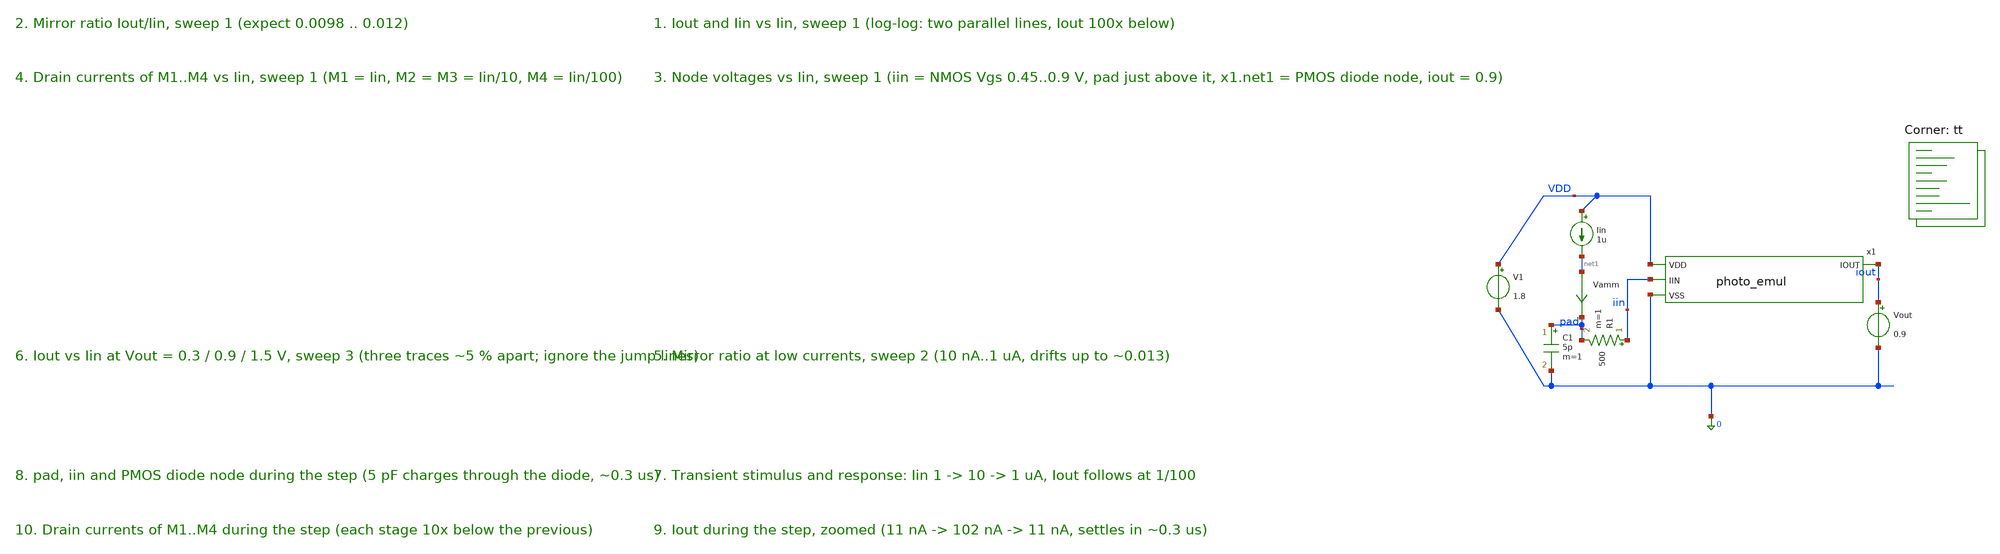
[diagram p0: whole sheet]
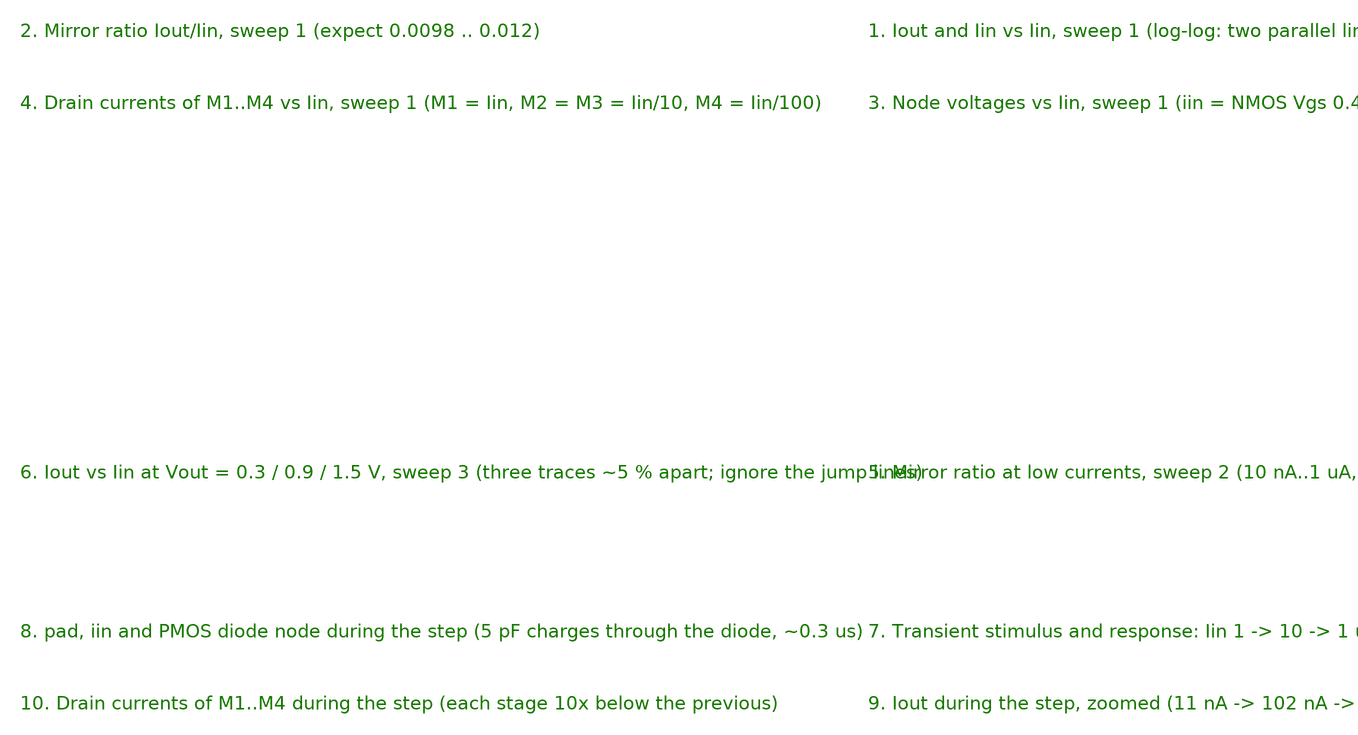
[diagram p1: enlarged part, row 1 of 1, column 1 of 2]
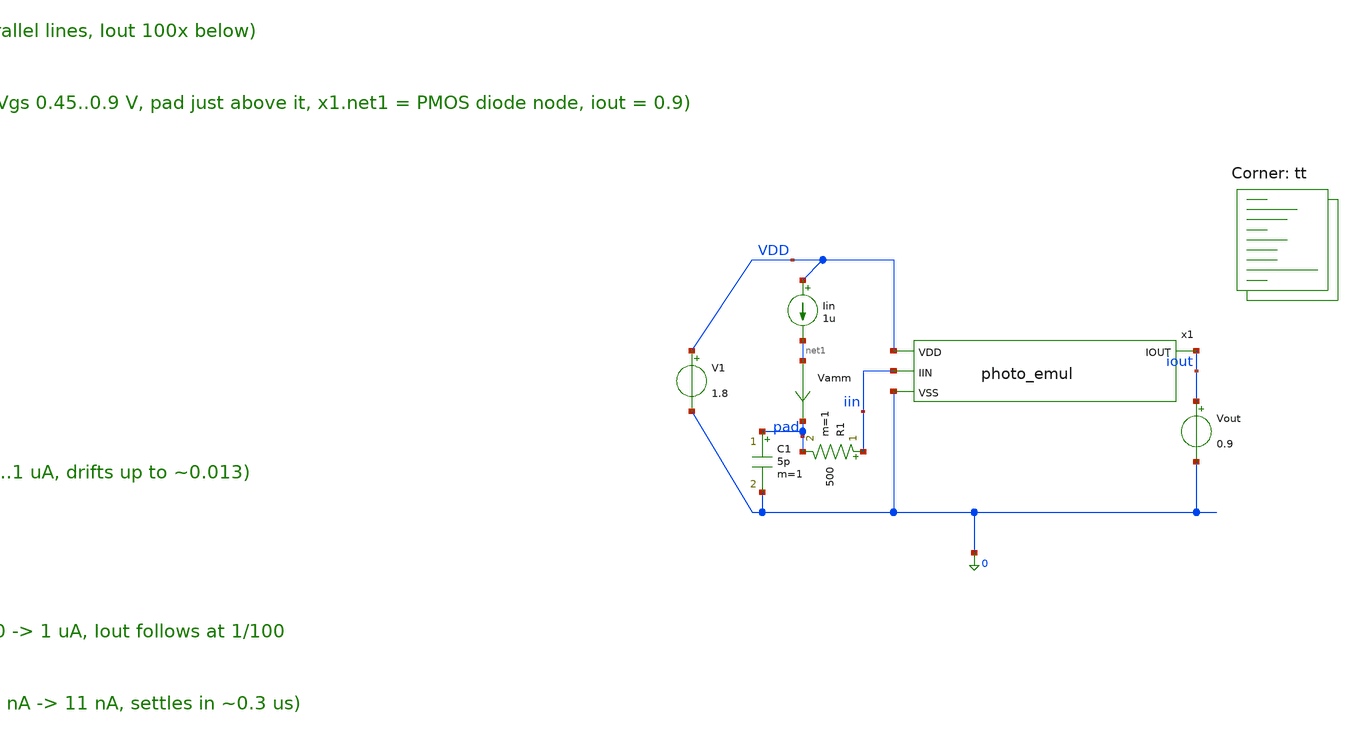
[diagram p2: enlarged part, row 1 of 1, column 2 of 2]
** sch_path: xschem/testbench_emul.sch
**.subckt testbench_emul
x1 VDD iin iout 0 photo_emul
Vamm net1 pad 0
.save i(vamm)
V1 VDD 0 1.8
Iin VDD net1 1u
Vout iout 0 0.9
R1 iin pad 500 m=1
C1 pad 0 5p m=1
**** begin user architecture code
.lib $::SKYWATER_MODELS/sky130.lib.spice tt


.option savecurrents
.control
save all
* sweep 1: input current 100 nA .. 100 uA (linear steps, log axes in the plots)
dc Iin 100n 100u 100n
plot abs(i(vout)) xlog ylog title 'Iout vs Iin (expect Iin/100)'
plot abs(i(vout))/abs(i(vamm)) xlog title 'mirror ratio Iout/Iin (expect 0.01)'
write testbench_emul.raw
set appendwrite
* sweep 2: low end, 10 nA .. 1 uA
dc Iin 10n 1u 10n
plot abs(i(vout))/abs(i(vamm)) xlog title 'mirror ratio at low currents'
write testbench_emul.raw
* sweep 3: same as 1 at Vout = 0.3, 0.9, 1.5 V
dc Iin 100n 100u 100n Vout 0.3 1.5 0.6
plot abs(i(vout)) xlog ylog title 'Iout at Vout = 0.3 / 0.9 / 1.5 V'
write testbench_emul.raw
* transient: step 1 -> 10 uA through the 500 ohm / 5 pF pin model
alter Iin dc = 1u
alter @Iin[pulse] = [ 1u 10u 1u 1n 1n 5u 10u ]
tran 10n 12u
plot v(pad) abs(i(vout)) title 'step through the pin model'
write testbench_emul.raw
.endc


**** end user architecture code
**.ends
.end
